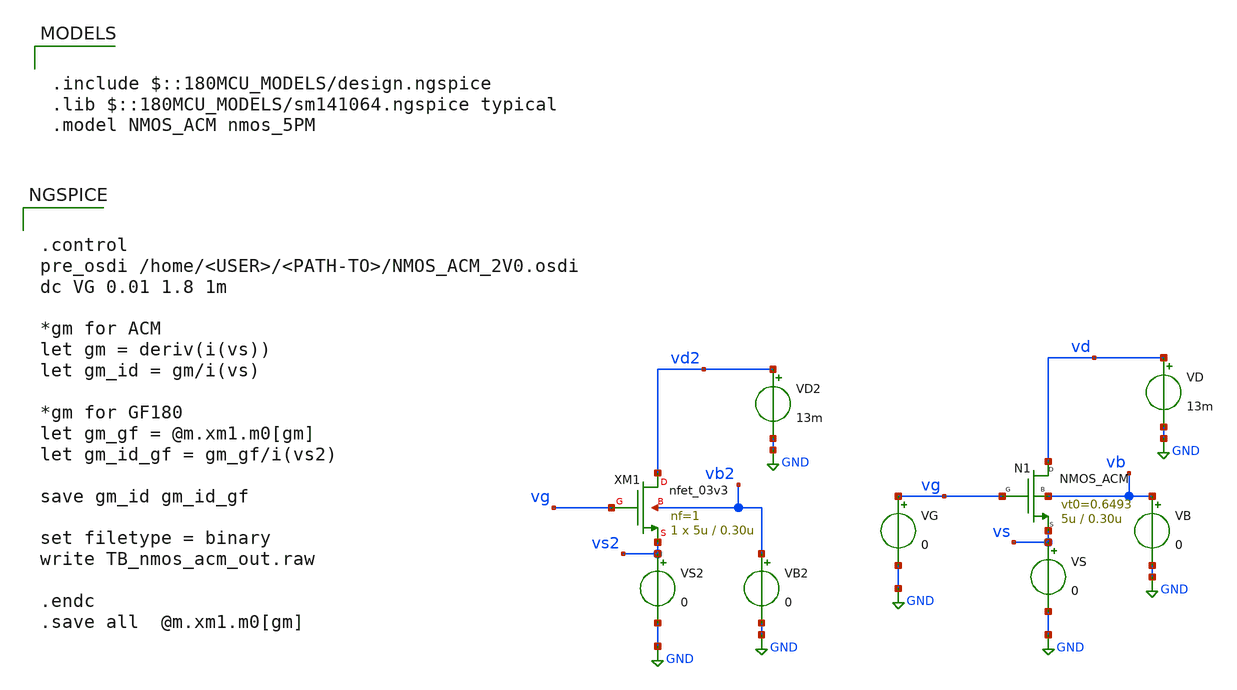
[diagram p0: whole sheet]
** sch_path: Examples/GF180MCU/xschem/TB_nmos_acm.sch
**.subckt TB_nmos_acm
VG vg GND 0
VD vd GND 13m
VB vb GND 0
VS vs GND 0
N1 vd vg vs vb NMOS_ACM w=5u l=0.30u n=1.383 is=1.076u vt0=0.6493 sigma=26m zeta=22m
XM1 vd2 vg vs2 vb2 nfet_03v3 L=0.30u W=5u nf=1 ad='int((nf+1)/2) * W/nf * 0.18u' as='int((nf+2)/2) * W/nf * 0.18u'
+ pd='2*int((nf+1)/2) * (W/nf + 0.18u)' ps='2*int((nf+2)/2) * (W/nf + 0.18u)' nrd='0.18u / W' nrs='0.18u / W'
+ sa=0 sb=0 sd=0 m=1
VD2 vd2 GND 13m
VB2 vb2 GND 0
VS2 vs2 GND 0
**** begin user architecture code

.include $::180MCU_MODELS/design.ngspice
.lib $::180MCU_MODELS/sm141064.ngspice typical
.model NMOS_ACM nmos_5PM



.control
pre_osdi /home/<USER>/<PATH-TO>/NMOS_ACM_2V0.osdi
dc VG 0.01 1.8 1m

*gm for ACM
let gm = deriv(i(vs))
let gm_id = gm/i(vs)

*gm for GF180
let gm_gf = @m.xm1.m0[gm]
let gm_id_gf = gm_gf/i(vs2)

save gm_id gm_id_gf

set filetype = binary
write TB_nmos_acm_out.raw

.endc
.save all  @m.xm1.m0[gm]


**** end user architecture code
**.ends
.GLOBAL GND
.end
